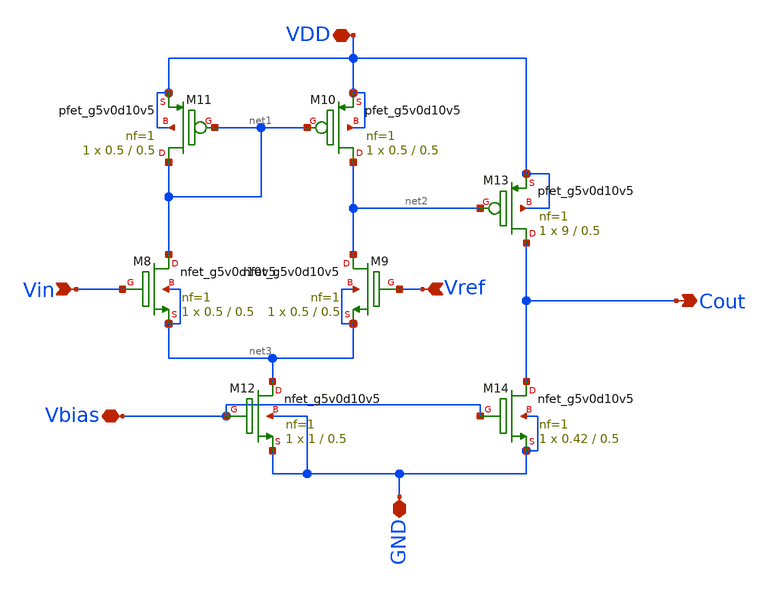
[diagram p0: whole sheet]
** sch_path: Analog Design Alan Rivera/Xschem/Sch/ComparadorFADC.sch
**.subckt ComparadorFADC Vin Cout VDD Vref GND Vbias
*.ipin Vin
*.opin Cout
*.iopin VDD
*.ipin Vref
*.iopin GND
*.iopin Vbias
XM8 net1 Vin net3 net3 sky130_fd_pr__nfet_g5v0d10v5 L=0.5 W=0.5 nf=1 ad='int((nf+1)/2) * W/nf * 0.29'
+ as='int((nf+2)/2) * W/nf * 0.29' pd='2*int((nf+1)/2) * (W/nf + 0.29)' ps='2*int((nf+2)/2) * (W/nf + 0.29)'
+ nrd='0.29 / W' nrs='0.29 / W' sa=0 sb=0 sd=0 mult=1 m=1
XM9 net2 Vref net3 net3 sky130_fd_pr__nfet_g5v0d10v5 L=0.5 W=0.5 nf=1 ad='int((nf+1)/2) * W/nf * 0.29'
+ as='int((nf+2)/2) * W/nf * 0.29' pd='2*int((nf+1)/2) * (W/nf + 0.29)' ps='2*int((nf+2)/2) * (W/nf + 0.29)'
+ nrd='0.29 / W' nrs='0.29 / W' sa=0 sb=0 sd=0 mult=1 m=1
XM10 net2 net1 VDD VDD sky130_fd_pr__pfet_g5v0d10v5 L=0.5 W=0.5 nf=1 ad='int((nf+1)/2) * W/nf * 0.29'
+ as='int((nf+2)/2) * W/nf * 0.29' pd='2*int((nf+1)/2) * (W/nf + 0.29)' ps='2*int((nf+2)/2) * (W/nf + 0.29)'
+ nrd='0.29 / W' nrs='0.29 / W' sa=0 sb=0 sd=0 mult=1 m=1
XM11 net1 net1 VDD VDD sky130_fd_pr__pfet_g5v0d10v5 L=0.5 W=0.5 nf=1 ad='int((nf+1)/2) * W/nf * 0.29'
+ as='int((nf+2)/2) * W/nf * 0.29' pd='2*int((nf+1)/2) * (W/nf + 0.29)' ps='2*int((nf+2)/2) * (W/nf + 0.29)'
+ nrd='0.29 / W' nrs='0.29 / W' sa=0 sb=0 sd=0 mult=1 m=1
XM12 net3 Vbias GND GND sky130_fd_pr__nfet_g5v0d10v5 L=0.5 W=1 nf=1 ad='int((nf+1)/2) * W/nf * 0.29'
+ as='int((nf+2)/2) * W/nf * 0.29' pd='2*int((nf+1)/2) * (W/nf + 0.29)' ps='2*int((nf+2)/2) * (W/nf + 0.29)'
+ nrd='0.29 / W' nrs='0.29 / W' sa=0 sb=0 sd=0 mult=1 m=1
XM13 Cout net2 VDD VDD sky130_fd_pr__pfet_g5v0d10v5 L=0.5 W=9 nf=1 ad='int((nf+1)/2) * W/nf * 0.29' as='int((nf+2)/2) * W/nf * 0.29'
+ pd='2*int((nf+1)/2) * (W/nf + 0.29)' ps='2*int((nf+2)/2) * (W/nf + 0.29)' nrd='0.29 / W' nrs='0.29 / W'
+ sa=0 sb=0 sd=0 mult=1 m=1
XM14 Cout Vbias GND GND sky130_fd_pr__nfet_g5v0d10v5 L=0.5 W=0.42 nf=1 ad='int((nf+1)/2) * W/nf * 0.29'
+ as='int((nf+2)/2) * W/nf * 0.29' pd='2*int((nf+1)/2) * (W/nf + 0.29)' ps='2*int((nf+2)/2) * (W/nf + 0.29)'
+ nrd='0.29 / W' nrs='0.29 / W' sa=0 sb=0 sd=0 mult=1 m=1
**.ends
.end
